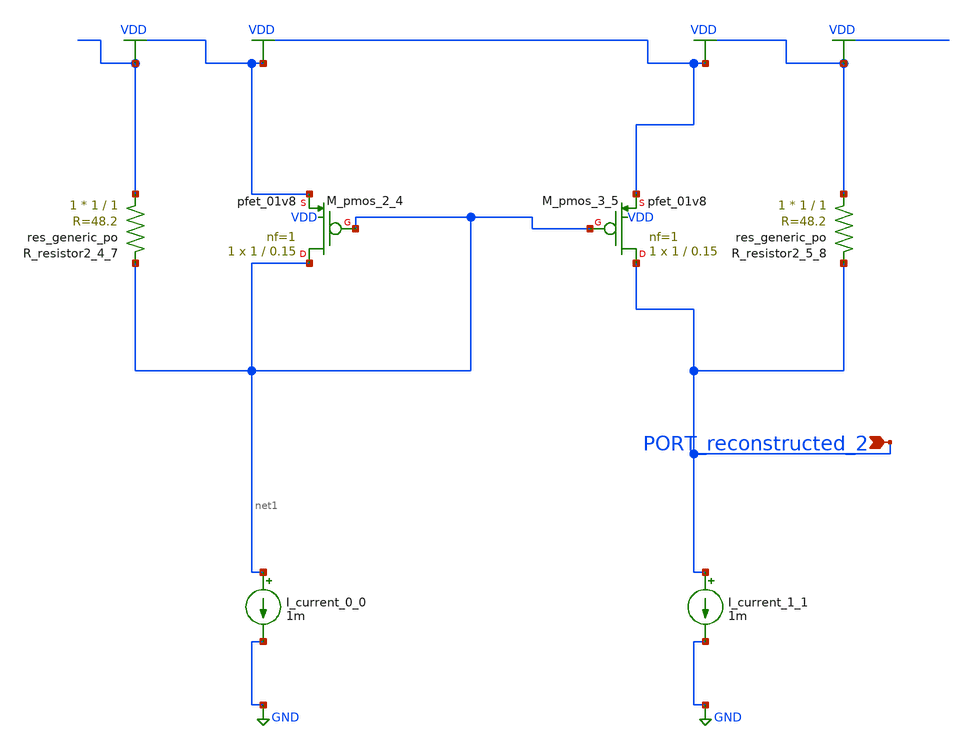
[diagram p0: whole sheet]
** sch_path: schematics/AMSNet/291.sch
**.subckt 291 PORT_reconstructed_2
*.ipin PORT_reconstructed_2
I_current_0_0 net1 GND 1m
I_current_1_1 PORT_reconstructed_2 GND 1m
XM_pmos_2_4 net1 net1 VDD VDD sky130_fd_pr__pfet_01v8 L=0.15 W=1 nf=1 ad='int((1 + 1)/2) * 1 / 1 * 0.29'
+ as='int((1 + 2)/2) * 1 / 1 * 0.29' pd='2*int((1 + 1)/2) * (1 / 1 + 0.29)' ps='2*int((1 + 2)/2) * (1 / 1 + 0.29)'
+ nrd='0.29 / 1 ' nrs='0.29 / 1 ' sa=0 sb=0 sd=0 mult=1 m=1
XM_pmos_3_5 PORT_reconstructed_2 net1 VDD VDD sky130_fd_pr__pfet_01v8 L=0.15 W=1 nf=1 ad='int((1 + 1)/2) * 1 / 1 * 0.29'
+ as='int((1 + 2)/2) * 1 / 1 * 0.29' pd='2*int((1 + 1)/2) * (1 / 1 + 0.29)' ps='2*int((1 + 2)/2) * (1 / 1 + 0.29)'
+ nrd='0.29 / 1 ' nrs='0.29 / 1 ' sa=0 sb=0 sd=0 mult=1 m=1
XR_resistor2_4_7 VDD net1 sky130_fd_pr__res_generic_po W=1 L=1 m=1
XR_resistor2_5_8 VDD PORT_reconstructed_2 sky130_fd_pr__res_generic_po W=1 L=1 m=1
**.ends
.GLOBAL GND
.GLOBAL VDD
.end
